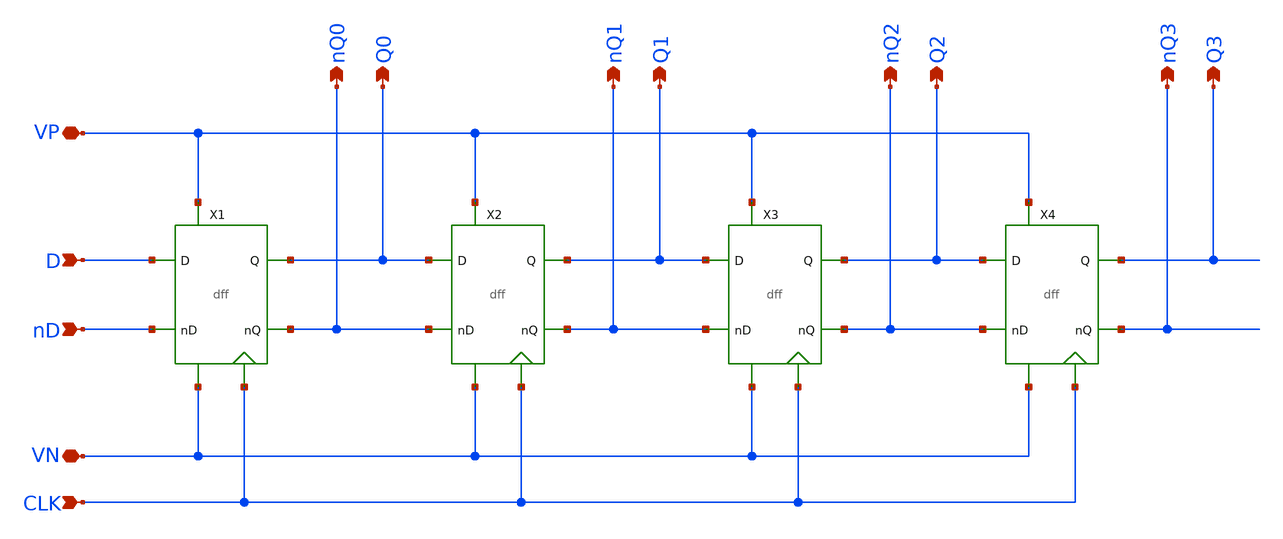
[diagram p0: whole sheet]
** sch_path: mini2/schem/shift_reg_4.sch
**.subckt shift_reg_4 nQ0 Q0 nQ1 Q1 nQ2 Q2 nQ3 Q3 CLK D nD VP VN
*.opin nQ0
*.opin Q0
*.opin nQ1
*.opin Q1
*.opin nQ2
*.opin Q2
*.opin nQ3
*.opin Q3
*.ipin CLK
*.ipin D
*.ipin nD
*.iopin VP
*.iopin VN
X1 Q0 nQ0 VN nD D VP CLK dff
X2 Q1 nQ1 VN nQ0 Q0 VP CLK dff
X3 Q2 nQ2 VN nQ1 Q1 VP CLK dff
X4 Q3 nQ3 VN nQ2 Q2 VP CLK dff
**.ends

* expanding   symbol:  /home/madvlsi/MADVLSI/mini2/schem/dff.sym # of pins=7
** sym_path: mini2/schem/dff.sym
** sch_path: mini2/schem/dff.sch
.subckt dff Q nQ VN nD D VP CLK
*.iopin VN
*.iopin VP
*.iopin VP
*.ipin D
*.ipin nD
*.ipin CLK
*.opin Q
*.opin nQ
XM1 net5 CLK D GND sky130_fd_pr__nfet_01v8 L=0.15 W=1 nf=1 ad='int((nf+1)/2) * W/nf * 0.29' as='int((nf+2)/2) * W/nf * 0.29'
+ pd='2*int((nf+1)/2) * (W/nf + 0.29)' ps='2*int((nf+2)/2) * (W/nf + 0.29)' nrd='0.29 / W' nrs='0.29 / W'
+ sa=0 sb=0 sd=0 mult=1 m=1
XM2 net6 CLK nD GND sky130_fd_pr__nfet_01v8 L=0.15 W=1 nf=1 ad='int((nf+1)/2) * W/nf * 0.29' as='int((nf+2)/2) * W/nf * 0.29'
+ pd='2*int((nf+1)/2) * (W/nf + 0.29)' ps='2*int((nf+2)/2) * (W/nf + 0.29)' nrd='0.29 / W' nrs='0.29 / W'
+ sa=0 sb=0 sd=0 mult=1 m=1
XM3 VN net6 net5 GND sky130_fd_pr__nfet_01v8 L=0.15 W=1 nf=1 ad='int((nf+1)/2) * W/nf * 0.29' as='int((nf+2)/2) * W/nf * 0.29'
+ pd='2*int((nf+1)/2) * (W/nf + 0.29)' ps='2*int((nf+2)/2) * (W/nf + 0.29)' nrd='0.29 / W' nrs='0.29 / W'
+ sa=0 sb=0 sd=0 mult=1 m=1
XM4 VN net5 net6 GND sky130_fd_pr__nfet_01v8 L=0.15 W=1 nf=1 ad='int((nf+1)/2) * W/nf * 0.29' as='int((nf+2)/2) * W/nf * 0.29'
+ pd='2*int((nf+1)/2) * (W/nf + 0.29)' ps='2*int((nf+2)/2) * (W/nf + 0.29)' nrd='0.29 / W' nrs='0.29 / W'
+ sa=0 sb=0 sd=0 mult=1 m=1
XM5 net4 CLK VP VDD sky130_fd_pr__pfet_01v8 L=0.15 W=1 nf=1 ad='int((nf+1)/2) * W/nf * 0.29' as='int((nf+2)/2) * W/nf * 0.29'
+ pd='2*int((nf+1)/2) * (W/nf + 0.29)' ps='2*int((nf+2)/2) * (W/nf + 0.29)' nrd='0.29 / W' nrs='0.29 / W'
+ sa=0 sb=0 sd=0 mult=1 m=1
XM6 net5 net6 net4 VDD sky130_fd_pr__pfet_01v8 L=0.15 W=1 nf=1 ad='int((nf+1)/2) * W/nf * 0.29' as='int((nf+2)/2) * W/nf * 0.29'
+ pd='2*int((nf+1)/2) * (W/nf + 0.29)' ps='2*int((nf+2)/2) * (W/nf + 0.29)' nrd='0.29 / W' nrs='0.29 / W'
+ sa=0 sb=0 sd=0 mult=1 m=1
XM7 net3 CLK VP VDD sky130_fd_pr__pfet_01v8 L=0.15 W=1 nf=1 ad='int((nf+1)/2) * W/nf * 0.29' as='int((nf+2)/2) * W/nf * 0.29'
+ pd='2*int((nf+1)/2) * (W/nf + 0.29)' ps='2*int((nf+2)/2) * (W/nf + 0.29)' nrd='0.29 / W' nrs='0.29 / W'
+ sa=0 sb=0 sd=0 mult=1 m=1
XM8 net6 net5 net3 VDD sky130_fd_pr__pfet_01v8 L=0.15 W=1 nf=1 ad='int((nf+1)/2) * W/nf * 0.29' as='int((nf+2)/2) * W/nf * 0.29'
+ pd='2*int((nf+1)/2) * (W/nf + 0.29)' ps='2*int((nf+2)/2) * (W/nf + 0.29)' nrd='0.29 / W' nrs='0.29 / W'
+ sa=0 sb=0 sd=0 mult=1 m=1
XM9 net1 CLK VN GND sky130_fd_pr__nfet_01v8 L=0.15 W=1 nf=1 ad='int((nf+1)/2) * W/nf * 0.29' as='int((nf+2)/2) * W/nf * 0.29'
+ pd='2*int((nf+1)/2) * (W/nf + 0.29)' ps='2*int((nf+2)/2) * (W/nf + 0.29)' nrd='0.29 / W' nrs='0.29 / W'
+ sa=0 sb=0 sd=0 mult=1 m=1
XM10 net2 CLK VN GND sky130_fd_pr__nfet_01v8 L=0.15 W=1 nf=1 ad='int((nf+1)/2) * W/nf * 0.29' as='int((nf+2)/2) * W/nf * 0.29'
+ pd='2*int((nf+1)/2) * (W/nf + 0.29)' ps='2*int((nf+2)/2) * (W/nf + 0.29)' nrd='0.29 / W' nrs='0.29 / W'
+ sa=0 sb=0 sd=0 mult=1 m=1
XM11 Q nQ net1 GND sky130_fd_pr__nfet_01v8 L=0.15 W=1 nf=1 ad='int((nf+1)/2) * W/nf * 0.29' as='int((nf+2)/2) * W/nf * 0.29'
+ pd='2*int((nf+1)/2) * (W/nf + 0.29)' ps='2*int((nf+2)/2) * (W/nf + 0.29)' nrd='0.29 / W' nrs='0.29 / W'
+ sa=0 sb=0 sd=0 mult=1 m=1
XM12 nQ Q net2 GND sky130_fd_pr__nfet_01v8 L=0.15 W=1 nf=1 ad='int((nf+1)/2) * W/nf * 0.29' as='int((nf+2)/2) * W/nf * 0.29'
+ pd='2*int((nf+1)/2) * (W/nf + 0.29)' ps='2*int((nf+2)/2) * (W/nf + 0.29)' nrd='0.29 / W' nrs='0.29 / W'
+ sa=0 sb=0 sd=0 mult=1 m=1
XM13 nQ CLK net5 VDD sky130_fd_pr__pfet_01v8 L=0.15 W=1 nf=1 ad='int((nf+1)/2) * W/nf * 0.29' as='int((nf+2)/2) * W/nf * 0.29'
+ pd='2*int((nf+1)/2) * (W/nf + 0.29)' ps='2*int((nf+2)/2) * (W/nf + 0.29)' nrd='0.29 / W' nrs='0.29 / W'
+ sa=0 sb=0 sd=0 mult=1 m=1
XM14 VP Q nQ VDD sky130_fd_pr__pfet_01v8 L=0.15 W=1 nf=1 ad='int((nf+1)/2) * W/nf * 0.29' as='int((nf+2)/2) * W/nf * 0.29'
+ pd='2*int((nf+1)/2) * (W/nf + 0.29)' ps='2*int((nf+2)/2) * (W/nf + 0.29)' nrd='0.29 / W' nrs='0.29 / W'
+ sa=0 sb=0 sd=0 mult=1 m=1
XM15 Q CLK net6 VDD sky130_fd_pr__pfet_01v8 L=0.15 W=1 nf=1 ad='int((nf+1)/2) * W/nf * 0.29' as='int((nf+2)/2) * W/nf * 0.29'
+ pd='2*int((nf+1)/2) * (W/nf + 0.29)' ps='2*int((nf+2)/2) * (W/nf + 0.29)' nrd='0.29 / W' nrs='0.29 / W'
+ sa=0 sb=0 sd=0 mult=1 m=1
XM16 VP nQ Q VDD sky130_fd_pr__pfet_01v8 L=0.15 W=1 nf=1 ad='int((nf+1)/2) * W/nf * 0.29' as='int((nf+2)/2) * W/nf * 0.29'
+ pd='2*int((nf+1)/2) * (W/nf + 0.29)' ps='2*int((nf+2)/2) * (W/nf + 0.29)' nrd='0.29 / W' nrs='0.29 / W'
+ sa=0 sb=0 sd=0 mult=1 m=1
.ends

.end
